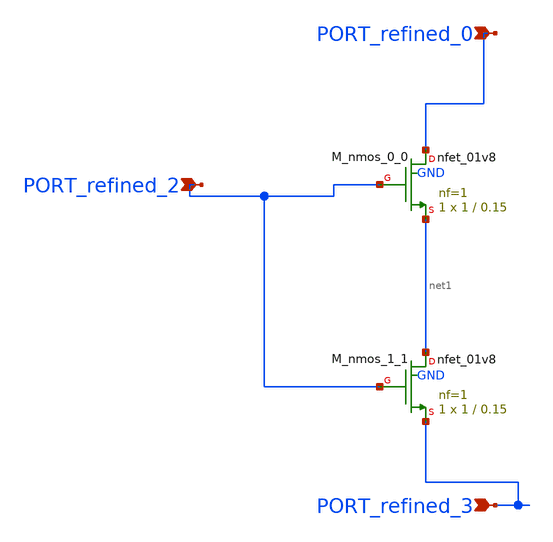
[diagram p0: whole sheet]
** sch_path: schematics/AMSNet/57.sch
**.subckt 57 PORT_refined_3 PORT_refined_2 PORT_refined_0
*.ipin PORT_refined_3
*.ipin PORT_refined_2
*.ipin PORT_refined_0
XM_nmos_0_0 PORT_refined_0 PORT_refined_2 net1 GND sky130_fd_pr__nfet_01v8 L=0.15 W=1 nf=1 ad='int((1 + 1)/2) * 1 / 1 * 0.29'
+ as='int((1 + 2)/2) * 1 / 1 * 0.29' pd='2*int((1 + 1)/2) * (1 / 1 + 0.29)' ps='2*int((1 + 2)/2) * (1 / 1 + 0.29)'
+ nrd='0.29 / 1 ' nrs='0.29 / 1 ' sa=0 sb=0 sd=0 mult=1 m=1
XM_nmos_1_1 net1 PORT_refined_2 PORT_refined_3 GND sky130_fd_pr__nfet_01v8 L=0.15 W=1 nf=1 ad='int((1 + 1)/2) * 1 / 1 * 0.29'
+ as='int((1 + 2)/2) * 1 / 1 * 0.29' pd='2*int((1 + 1)/2) * (1 / 1 + 0.29)' ps='2*int((1 + 2)/2) * (1 / 1 + 0.29)'
+ nrd='0.29 / 1 ' nrs='0.29 / 1 ' sa=0 sb=0 sd=0 mult=1 m=1
**.ends
.end
